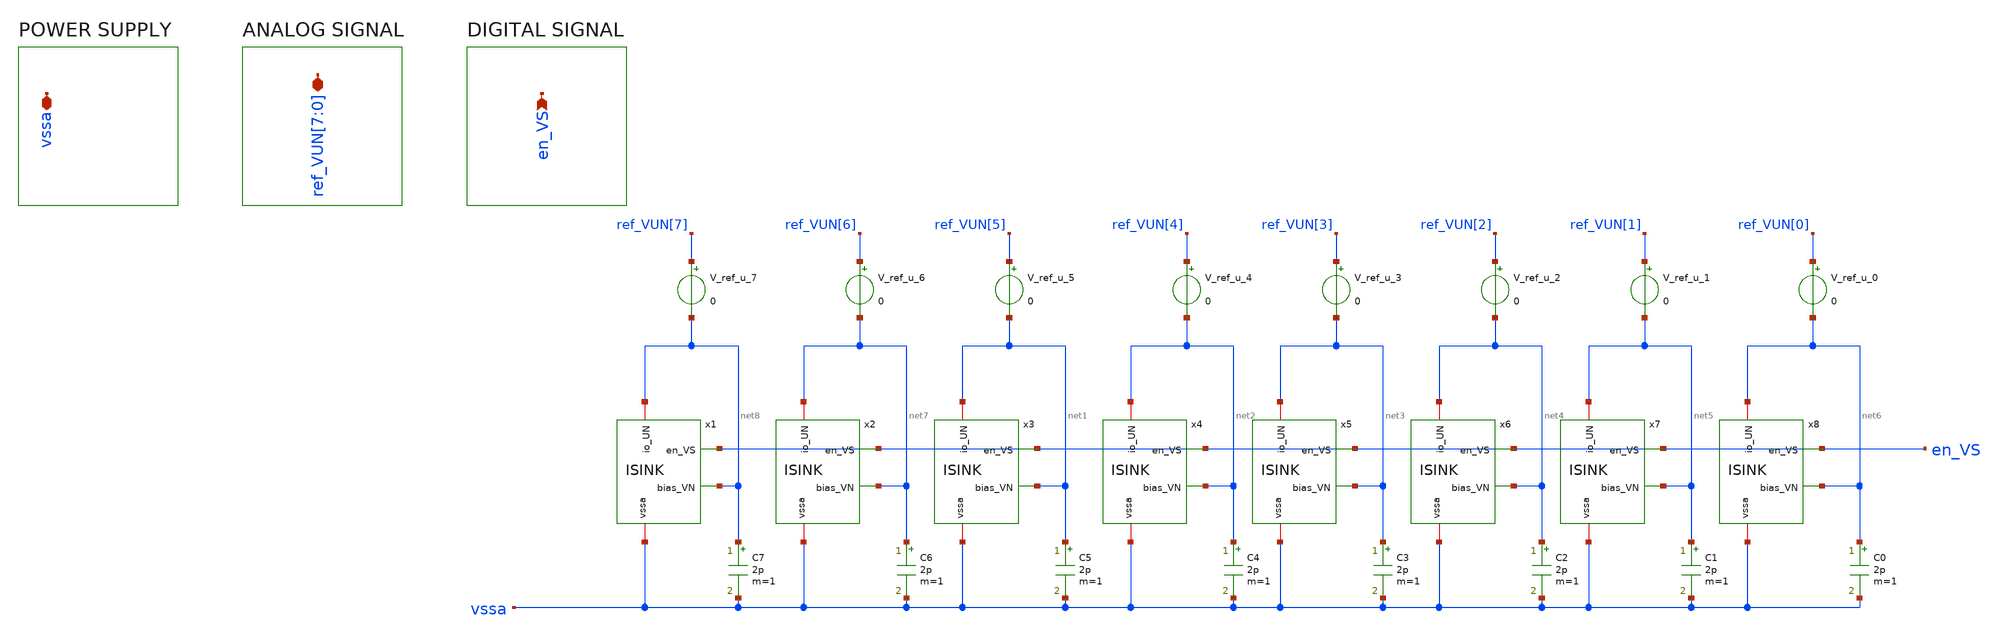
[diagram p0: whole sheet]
** sch_path: CoreDiodeT.sch
**.subckt CoreDiodeT
*+ ref_VUN[7],ref_VUN[6],ref_VUN[5],ref_VUN[4],ref_VUN[3],ref_VUN[2],ref_VUN[1],ref_VUN[0] en_VS vssa
*.iopin ref_VUN[7],ref_VUN[6],ref_VUN[5],ref_VUN[4],ref_VUN[3],ref_VUN[2],ref_VUN[1],ref_VUN[0]
*.ipin en_VS
*.iopin vssa
x1 net8 vssa en_VS net8 ISINK
x2 net7 vssa en_VS net7 ISINK
x3 net1 vssa en_VS net1 ISINK
x4 net2 vssa en_VS net2 ISINK
x5 net3 vssa en_VS net3 ISINK
x6 net4 vssa en_VS net4 ISINK
x7 net5 vssa en_VS net5 ISINK
x8 net6 vssa en_VS net6 ISINK
C0 net6 vssa 2p m=1
C1 net5 vssa 2p m=1
C2 net4 vssa 2p m=1
C3 net3 vssa 2p m=1
C4 net2 vssa 2p m=1
C5 net1 vssa 2p m=1
C6 net7 vssa 2p m=1
C7 net8 vssa 2p m=1
V_ref_u_0 ref_VUN[0] net6 0
V_ref_u_1 ref_VUN[1] net5 0
V_ref_u_2 ref_VUN[2] net4 0
V_ref_u_3 ref_VUN[3] net3 0
V_ref_u_4 ref_VUN[4] net2 0
V_ref_u_5 ref_VUN[5] net1 0
V_ref_u_6 ref_VUN[6] net7 0
V_ref_u_7 ref_VUN[7] net8 0
**.ends

* expanding   symbol:  ISINK.sym # of pins=4
** sym_path: ISINK.sym
** sch_path: ISINK.sch
.subckt ISINK bias_VN vssa en_VS io_UN
*.ipin en_VS
*.iopin vssa
*.ipin bias_VN
*.iopin io_UN
XM1 io_UN en_VS net2 vssa sg13_hv_nmos w=2.5u l=0.5u ng=1 m=1 mm_ok=1
XM2 net2 bias_VN net1 vssa sg13_hv_nmos w=1u l=2u ng=1 m=1 mm_ok=1
XM3 net1 bias_VN vssa vssa sg13_hv_nmos w=1u l=2u ng=1 m=1 mm_ok=1
.ends

.end
